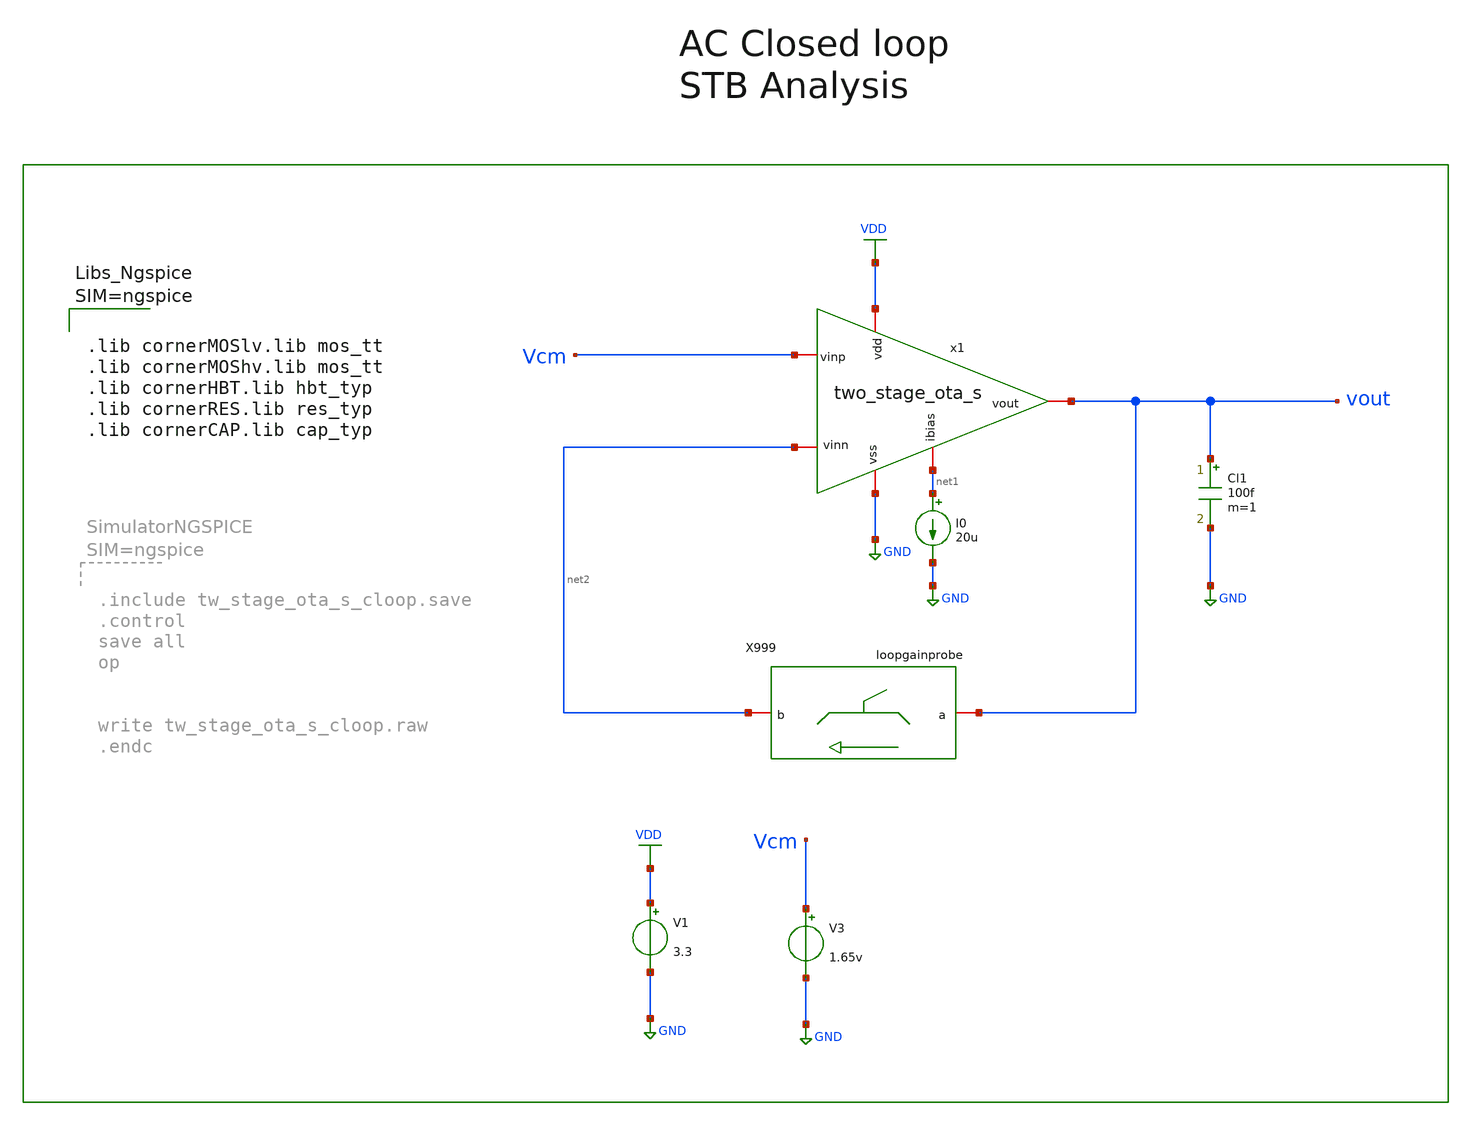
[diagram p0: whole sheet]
** sch_path: dependencies/pmu_ip/dependencies/OTA/OTA-main/testbenches/tw_stage_ota_s_cloop.sch
* (c) 2025-2026 Ider Abdelaziz
**.subckt tw_stage_ota_s_cloop
I0 net1 GND 20u
V1 VDD GND 3.3
V3 Vcm GND 1.65v
Cl1 vout GND 100f m=1
X999 vout net2 loopgainprobe
x1 VDD net1 net2 Vcm vout GND two_stage_ota_s
**** begin user architecture code



.lib cornerMOSlv.lib mos_tt
.lib cornerMOShv.lib mos_tt
.lib cornerHBT.lib hbt_typ
.lib cornerRES.lib res_typ
.lib cornerCAP.lib cap_typ





.include  /foss/designs/bandgap_refrence_ihp/ITI_Analog/Misc/LoopGainProbe/stb.spi




**** end user architecture code
**.ends
.GLOBAL GND
.GLOBAL VDD
.end
